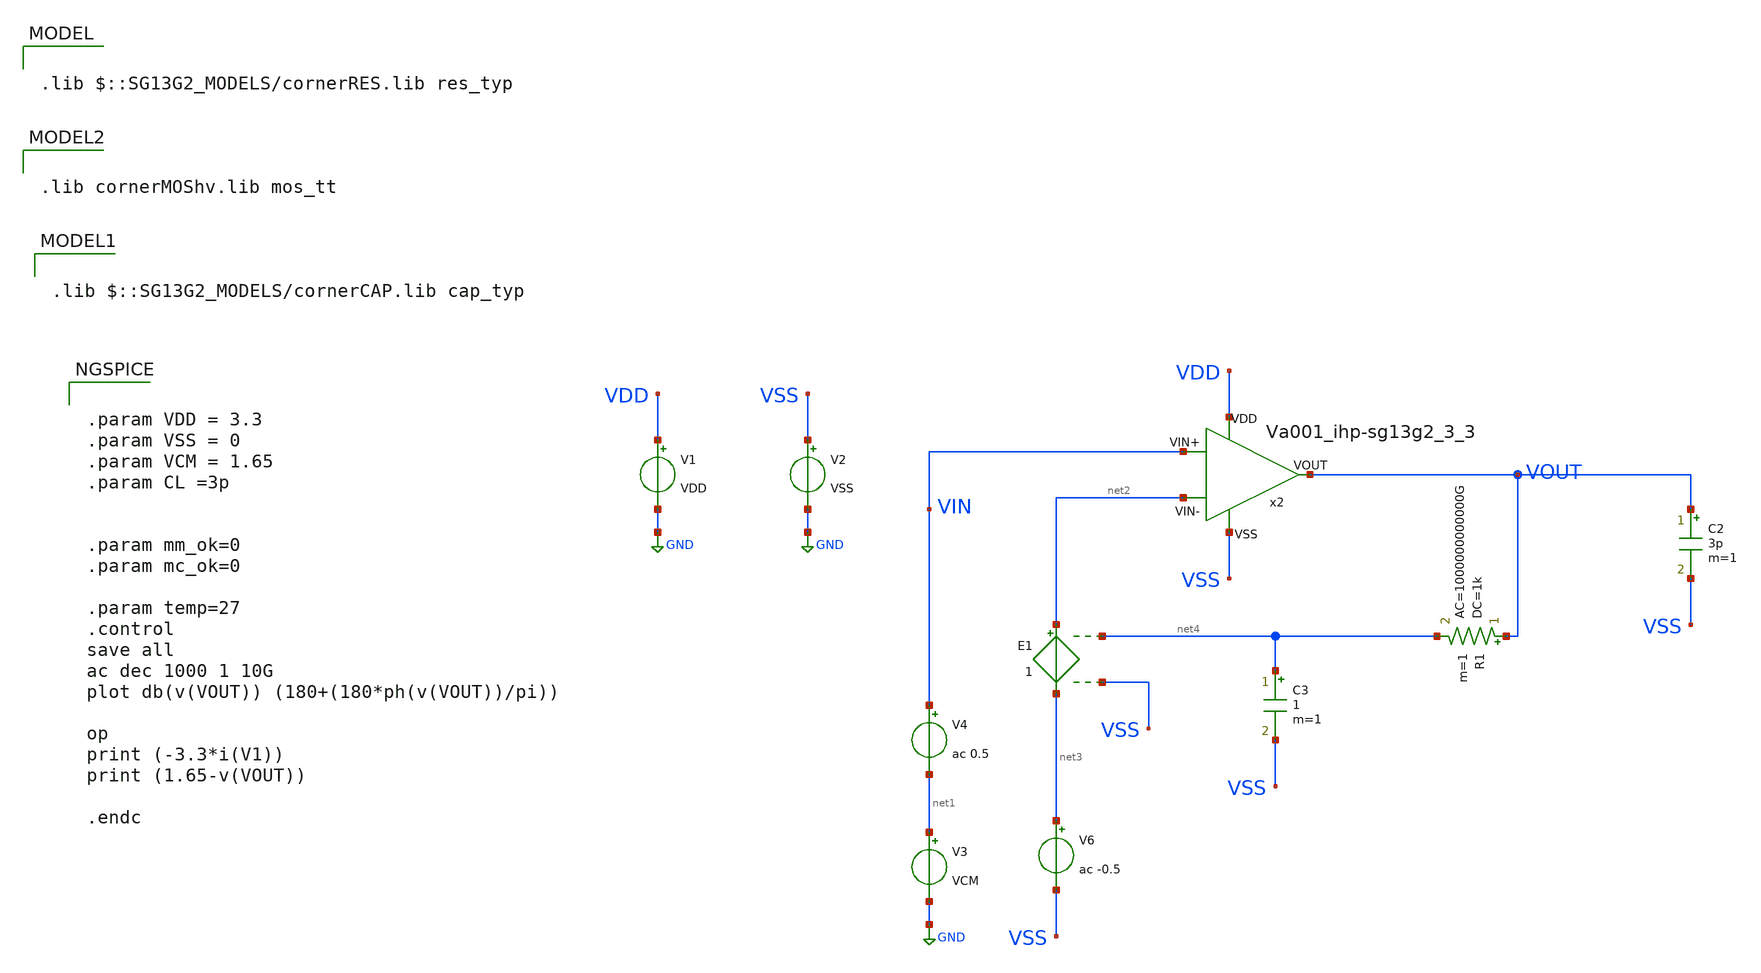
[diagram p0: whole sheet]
** sch_path: Learning/single_ended_amplifiers/VA001_series/Design_and_Analysis_of_Two-Stage_CMOS_Operational_Amplifier_for_Fluorescence_Signal_Processing_ihp130_3_3V/amplifier_design/single_tb.sch
**.subckt single_tb
V1 VDD GND VDD
V2 VSS GND VSS
V3 net1 GND VCM
V4 VIN net1 ac 0.5
V6 net3 VSS ac -0.5
E1 net2 net3 net4 VSS 1
C2 VOUT VSS 3p m=1
R1 VOUT net4 1k ac=1000000000000G m=1
C3 net4 VSS 1 m=1
x2 VDD VSS net2 VIN VOUT Va001_ihp-sg13g2_3_3
**** begin user architecture code

.lib $::SG13G2_MODELS/cornerRES.lib res_typ


.lib cornerMOShv.lib mos_tt


.lib $::SG13G2_MODELS/cornerCAP.lib cap_typ

**** end user architecture code
**.ends

* expanding   symbol:  ihp-sg13g2/Amplifiers/Va001_ihp-sg13g2_3_3.sym # of pins=5
** sym_path: LIB/ihp-sg13g2/Amplifiers/Va001_ihp-sg13g2_3_3.sym
** sch_path: LIB/ihp-sg13g2/Amplifiers/Va001_ihp-sg13g2_3_3.sch
.subckt Va001_ihp-sg13g2_3_3 VDD VSS VIN- VIN+ VOUT
*.iopin VDD
*.iopin VSS
*.iopin VIN-
*.iopin VIN+
*.iopin VOUT
XM2 VB1 VB1 VDD VDD sg13_hv_pmos w=1.5u l=2u ng=2 m=2 mm_ok=1
XM1 VB2 VB1 VDD VDD sg13_hv_pmos w=1.5u l=2u ng=2 m=2 mm_ok=1
XM3 VB1 VB2 net3 VSS sg13_hv_nmos w=1.0u l=2u ng=2 m=2 mm_ok=1
XM4 VB2 VB2 net1 VSS sg13_hv_nmos w=1.0u l=2u ng=2 m=2 mm_ok=1
XM5 net3 net1 net2 VSS sg13_hv_nmos w=2u l=2u ng=2 m=8 mm_ok=1
XM6 net1 net1 VSS VSS sg13_hv_nmos w=2u l=2u ng=2 m=2 mm_ok=1
XR1 net2 VSS sub! rhigh w=0.5e-6 l=5.9e-6 m=1 b=0 mm_ok=1
XM7 net4 VB1 VDD VDD sg13_hv_pmos w=1.5u l=2u ng=2 m=8 mm_ok=1
XM9 net6 VIN+ net4 net4 sg13_hv_pmos w=8u l=0.8u ng=4 m=4 mm_ok=1
XM8 net5 VIN- net4 net4 sg13_hv_pmos w=8u l=0.8u ng=4 m=4 mm_ok=1
XM10 net5 net5 VSS VSS sg13_hv_nmos w=2u l=2u ng=2 m=2 mm_ok=1
XM11 net6 net5 VSS VSS sg13_hv_nmos w=2u l=2u ng=2 m=2 mm_ok=1
XM12 VOUT VB1 VDD VDD sg13_hv_pmos w=1.5u l=2u ng=2 m=16 mm_ok=1
XM13 VOUT net6 VSS VSS sg13_hv_nmos w=2u l=0.8u ng=2 m=4 mm_ok=1
XM14 net6 VB2 net7 VSS sg13_hv_nmos w=2u l=2.7u ng=1 m=2 mm_ok=1
XC1 VOUT net7 cap_cmim w=9e-6 l=9e-6 m=4 mm_ok=1
.ends

.GLOBAL GND
**** begin user architecture code


.param VDD = 3.3
.param VSS = 0
.param VCM = 1.65
.param CL =3p


.param mm_ok=0
.param mc_ok=0

.param temp=27
.control
save all
ac dec 1000 1 10G
plot db(v(VOUT)) (180+(180*ph(v(VOUT))/pi))

op
print (-3.3*i(V1))
print (1.65-v(VOUT))

.endc


**** end user architecture code
.end
